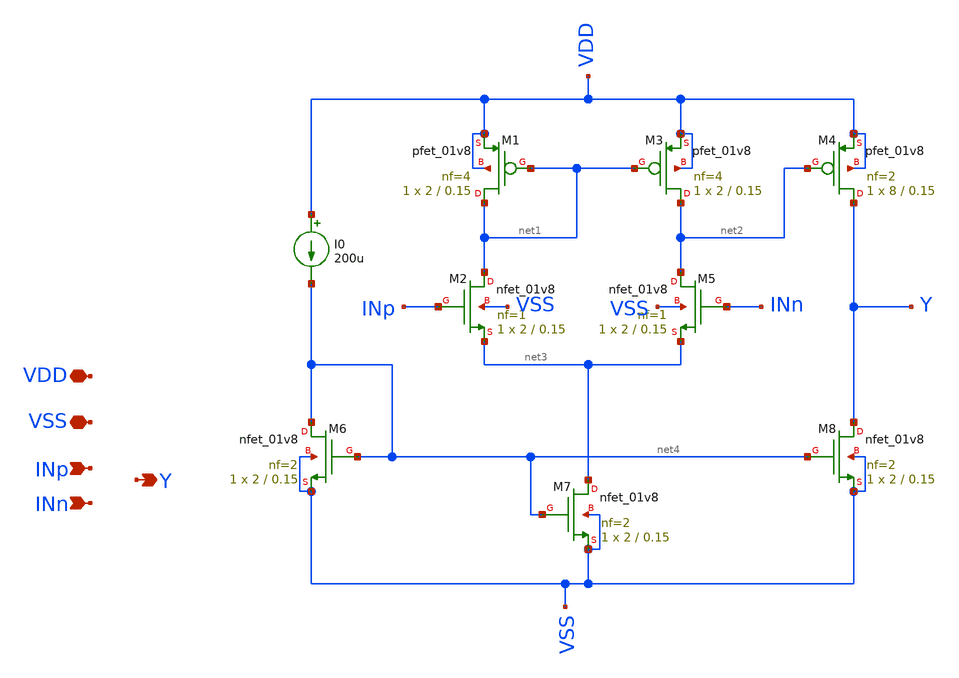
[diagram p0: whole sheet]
** sch_path: xschem/src/amp2.sch
**.subckt amp2 Y VSS INp INn VDD
*.opin Y
*.iopin VSS
*.ipin INp
*.ipin INn
*.iopin VDD
XM1 net1 net1 VDD VDD sky130_fd_pr__pfet_01v8 L=0.15 W=2 nf=4 ad='int((nf+1)/2) * W/nf * 0.29' as='int((nf+2)/2) * W/nf * 0.29'
+ pd='2*int((nf+1)/2) * (W/nf + 0.29)' ps='2*int((nf+2)/2) * (W/nf + 0.29)' nrd='0.29 / W' nrs='0.29 / W'
+ sa=0 sb=0 sd=0 mult=1 m=1
XM2 net1 INp net3 VSS sky130_fd_pr__nfet_01v8 L=0.15 W=2 nf=1 ad='int((nf+1)/2) * W/nf * 0.29' as='int((nf+2)/2) * W/nf * 0.29'
+ pd='2*int((nf+1)/2) * (W/nf + 0.29)' ps='2*int((nf+2)/2) * (W/nf + 0.29)' nrd='0.29 / W' nrs='0.29 / W'
+ sa=0 sb=0 sd=0 mult=1 m=1
XM3 net2 net1 VDD VDD sky130_fd_pr__pfet_01v8 L=0.15 W=2 nf=4 ad='int((nf+1)/2) * W/nf * 0.29' as='int((nf+2)/2) * W/nf * 0.29'
+ pd='2*int((nf+1)/2) * (W/nf + 0.29)' ps='2*int((nf+2)/2) * (W/nf + 0.29)' nrd='0.29 / W' nrs='0.29 / W'
+ sa=0 sb=0 sd=0 mult=1 m=1
XM4 Y net2 VDD VDD sky130_fd_pr__pfet_01v8 L=0.15 W=8 nf=2 ad='int((nf+1)/2) * W/nf * 0.29' as='int((nf+2)/2) * W/nf * 0.29'
+ pd='2*int((nf+1)/2) * (W/nf + 0.29)' ps='2*int((nf+2)/2) * (W/nf + 0.29)' nrd='0.29 / W' nrs='0.29 / W'
+ sa=0 sb=0 sd=0 mult=1 m=1
XM5 net2 INn net3 VSS sky130_fd_pr__nfet_01v8 L=0.15 W=2 nf=1 ad='int((nf+1)/2) * W/nf * 0.29' as='int((nf+2)/2) * W/nf * 0.29'
+ pd='2*int((nf+1)/2) * (W/nf + 0.29)' ps='2*int((nf+2)/2) * (W/nf + 0.29)' nrd='0.29 / W' nrs='0.29 / W'
+ sa=0 sb=0 sd=0 mult=1 m=1
XM6 net4 net4 VSS VSS sky130_fd_pr__nfet_01v8 L=0.15 W=2 nf=2 ad='int((nf+1)/2) * W/nf * 0.29' as='int((nf+2)/2) * W/nf * 0.29'
+ pd='2*int((nf+1)/2) * (W/nf + 0.29)' ps='2*int((nf+2)/2) * (W/nf + 0.29)' nrd='0.29 / W' nrs='0.29 / W'
+ sa=0 sb=0 sd=0 mult=1 m=1
XM7 net3 net4 VSS VSS sky130_fd_pr__nfet_01v8 L=0.15 W=2 nf=2 ad='int((nf+1)/2) * W/nf * 0.29' as='int((nf+2)/2) * W/nf * 0.29'
+ pd='2*int((nf+1)/2) * (W/nf + 0.29)' ps='2*int((nf+2)/2) * (W/nf + 0.29)' nrd='0.29 / W' nrs='0.29 / W'
+ sa=0 sb=0 sd=0 mult=1 m=1
XM8 Y net4 VSS VSS sky130_fd_pr__nfet_01v8 L=0.15 W=2 nf=2 ad='int((nf+1)/2) * W/nf * 0.29' as='int((nf+2)/2) * W/nf * 0.29'
+ pd='2*int((nf+1)/2) * (W/nf + 0.29)' ps='2*int((nf+2)/2) * (W/nf + 0.29)' nrd='0.29 / W' nrs='0.29 / W'
+ sa=0 sb=0 sd=0 mult=1 m=1
I0 VDD net4 200u
**.ends
.end
